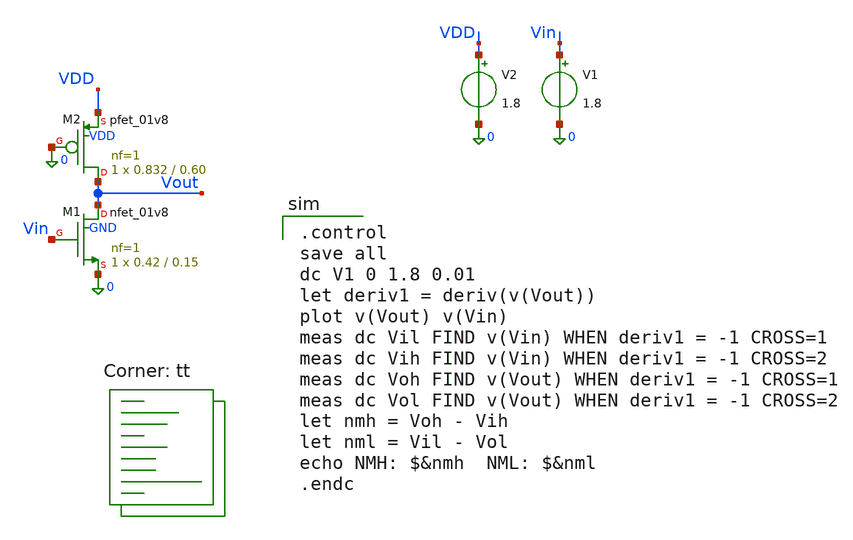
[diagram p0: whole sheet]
** sch_path: tutorial-2/source/q2b.sch
**.subckt q2b
V1 Vin 0 1.8
XM1 Vout Vin 0 GND sky130_fd_pr__nfet_01v8 L=0.15 W=0.42 nf=1 ad='int((nf+1)/2) * W/nf * 0.29' as='int((nf+2)/2) * W/nf * 0.29'
+ pd='2*int((nf+1)/2) * (W/nf + 0.29)' ps='2*int((nf+2)/2) * (W/nf + 0.29)' nrd='0.29 / W' nrs='0.29 / W'
+ sa=0 sb=0 sd=0 mult=1 m=1
XM2 Vout 0 VDD VDD sky130_fd_pr__pfet_01v8 L=0.60 W=0.832 nf=1 ad='int((nf+1)/2) * W/nf * 0.29' as='int((nf+2)/2) * W/nf * 0.29'
+ pd='2*int((nf+1)/2) * (W/nf + 0.29)' ps='2*int((nf+2)/2) * (W/nf + 0.29)' nrd='0.29 / W' nrs='0.29 / W'
+ sa=0 sb=0 sd=0 mult=1 m=1
V2 VDD 0 1.8
**** begin user architecture code
.lib $::SKYWATER_MODELS/sky130.lib.spice tt

.control
save all
dc V1 0 1.8 0.01
let deriv1 = deriv(v(Vout))
plot v(Vout) v(Vin)
meas dc Vil FIND v(Vin) WHEN deriv1 = -1 CROSS=1
meas dc Vih FIND v(Vin) WHEN deriv1 = -1 CROSS=2
meas dc Voh FIND v(Vout) WHEN deriv1 = -1 CROSS=1
meas dc Vol FIND v(Vout) WHEN deriv1 = -1 CROSS=2
let nmh = Voh - Vih
let nml = Vil - Vol
echo NMH: $&nmh  NML: $&nml
.endc

**** end user architecture code
**.ends
.end
